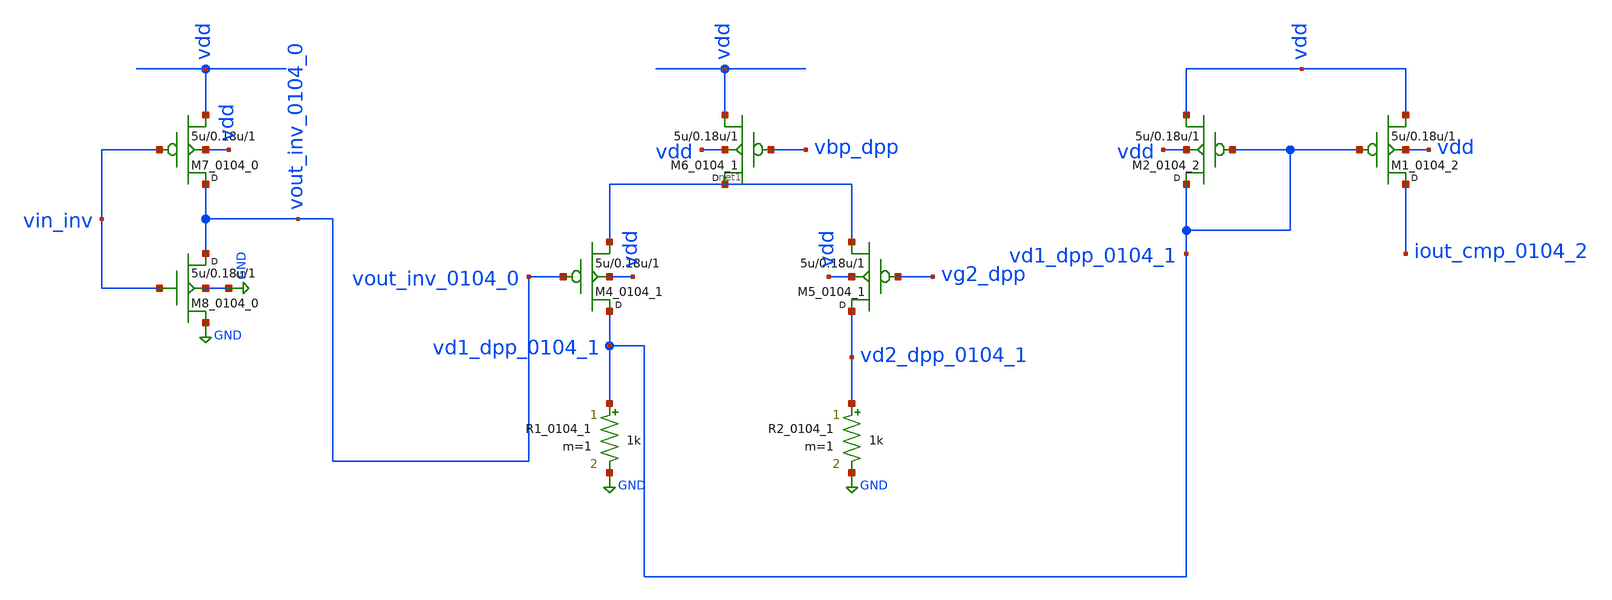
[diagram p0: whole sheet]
** sch_path: synthetic/generated/0104_generated.sch
**.subckt 0104_generated
M7_0104_0 vout_inv_0104_0 vin_inv vdd vdd pmos w=5u l=0.18u m=1
M8_0104_0 vout_inv_0104_0 vin_inv GND GND nmos w=5u l=0.18u m=1
M4_0104_1 vd1_dpp_0104_1 vout_inv_0104_0 net1 vdd pmos w=5u l=0.18u m=1
M5_0104_1 vd2_dpp_0104_1 vg2_dpp net1 vdd pmos w=5u l=0.18u m=1
M6_0104_1 net1 vbp_dpp vdd vdd pmos w=5u l=0.18u m=1
R1_0104_1 vd1_dpp_0104_1 GND 1k m=1
R2_0104_1 vd2_dpp_0104_1 GND 1k m=1
M1_0104_2 iout_cmp_0104_2 vd1_dpp_0104_1 vdd vdd pmos w=5u l=0.18u m=1
M2_0104_2 vd1_dpp_0104_1 vd1_dpp_0104_1 vdd vdd pmos w=5u l=0.18u m=1
**.ends
.GLOBAL GND
.end
